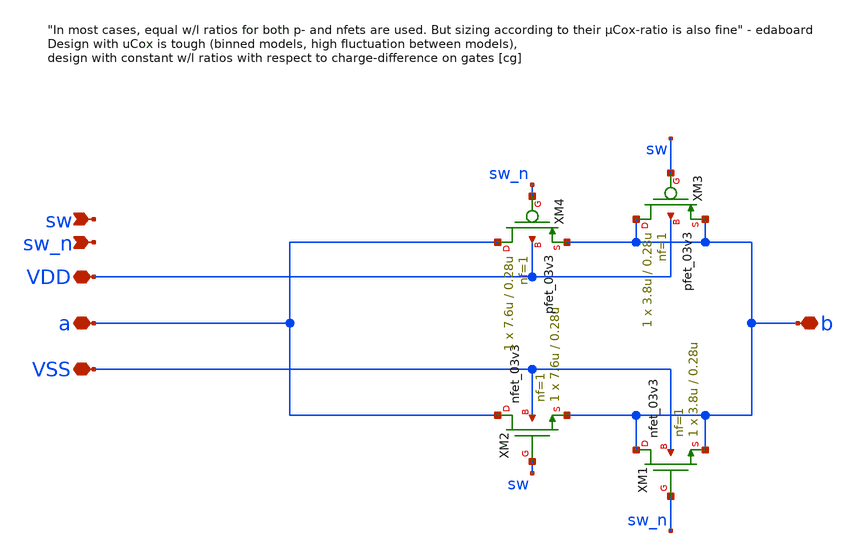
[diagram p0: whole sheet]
** sch_path: adc_sar_switch_gate.sch
**.subckt adc_sar_switch_gate VSS VDD sw_n sw a b
*.iopin VSS
*.iopin VDD
*.ipin sw_n
*.ipin sw
*.iopin a
*.iopin b
XM1 b sw_n b VSS nfet_03v3 L=0.28u W=3.8u nf=1 ad='int((nf+1)/2) * W/nf * 0.18u' as='int((nf+2)/2) * W/nf * 0.18u'
+ pd='2*int((nf+1)/2) * (W/nf + 0.18u)' ps='2*int((nf+2)/2) * (W/nf + 0.18u)' nrd='0.18u / W' nrs='0.18u / W'
+ sa=0 sb=0 sd=0 m=1
XM2 a sw b VSS nfet_03v3 L=0.28u W=7.6u nf=1 ad='int((nf+1)/2) * W/nf * 0.18u' as='int((nf+2)/2) * W/nf * 0.18u'
+ pd='2*int((nf+1)/2) * (W/nf + 0.18u)' ps='2*int((nf+2)/2) * (W/nf + 0.18u)' nrd='0.18u / W' nrs='0.18u / W'
+ sa=0 sb=0 sd=0 m=1
XM3 b sw b VDD pfet_03v3 L=0.28u W=3.8u nf=1 ad='int((nf+1)/2) * W/nf * 0.18u' as='int((nf+2)/2) * W/nf * 0.18u'
+ pd='2*int((nf+1)/2) * (W/nf + 0.18u)' ps='2*int((nf+2)/2) * (W/nf + 0.18u)' nrd='0.18u / W' nrs='0.18u / W'
+ sa=0 sb=0 sd=0 m=1
XM4 a sw_n b VDD pfet_03v3 L=0.28u W=7.6u nf=1 ad='int((nf+1)/2) * W/nf * 0.18u' as='int((nf+2)/2) * W/nf * 0.18u'
+ pd='2*int((nf+1)/2) * (W/nf + 0.18u)' ps='2*int((nf+2)/2) * (W/nf + 0.18u)' nrd='0.18u / W' nrs='0.18u / W'
+ sa=0 sb=0 sd=0 m=1
**.ends
.end
